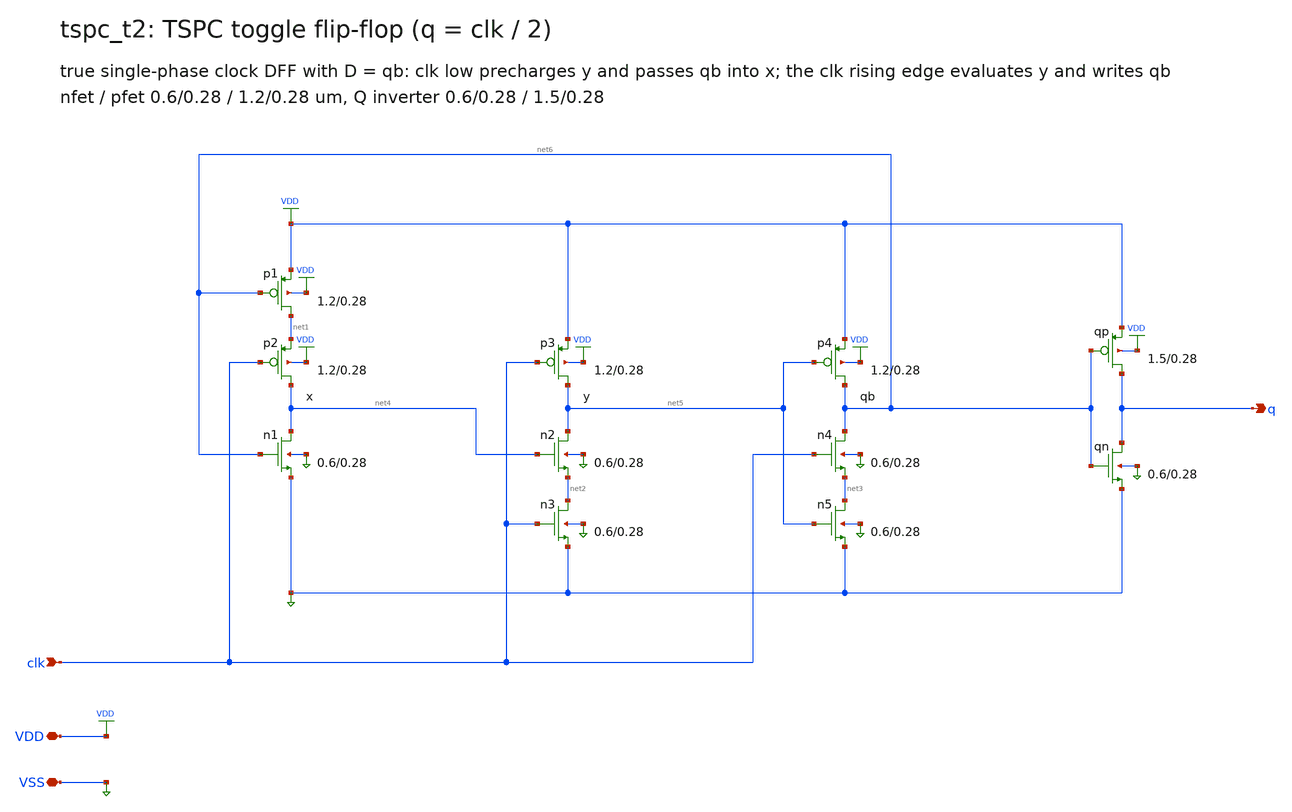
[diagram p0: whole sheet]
** sch_path: xschem/tspc_t2.sch
**.subckt tspc_t2 VDD VSS clk q
*.iopin VDD
*.iopin VSS
*.ipin clk
*.opin q
Xp1 net1 net6 VDD VDD pfet_03v3 L=0.28u W=1.2u nf=1 ad=0.6p as=0.6p pd=3.4u ps=3.4u nrd=0 nrs=0 sa=0
+ sb=0 sd=0 m=1
Xp2 net4 clk net1 VDD pfet_03v3 L=0.28u W=1.2u nf=1 ad=0.6p as=0.6p pd=3.4u ps=3.4u nrd=0 nrs=0 sa=0
+ sb=0 sd=0 m=1
Xn1 net4 net6 VSS VSS nfet_03v3 L=0.28u W=0.6u nf=1 ad=0.3p as=0.3p pd=2.2u ps=2.2u nrd=0 nrs=0 sa=0
+ sb=0 sd=0 m=1
Xp3 net5 clk VDD VDD pfet_03v3 L=0.28u W=1.2u nf=1 ad=0.6p as=0.6p pd=3.4u ps=3.4u nrd=0 nrs=0 sa=0
+ sb=0 sd=0 m=1
Xn2 net5 net4 net2 VSS nfet_03v3 L=0.28u W=0.6u nf=1 ad=0.3p as=0.3p pd=2.2u ps=2.2u nrd=0 nrs=0
+ sa=0 sb=0 sd=0 m=1
Xn3 net2 clk VSS VSS nfet_03v3 L=0.28u W=0.6u nf=1 ad=0.3p as=0.3p pd=2.2u ps=2.2u nrd=0 nrs=0 sa=0
+ sb=0 sd=0 m=1
Xp4 net6 net5 VDD VDD pfet_03v3 L=0.28u W=1.2u nf=1 ad=0.6p as=0.6p pd=3.4u ps=3.4u nrd=0 nrs=0 sa=0
+ sb=0 sd=0 m=1
Xn4 net6 clk net3 VSS nfet_03v3 L=0.28u W=0.6u nf=1 ad=0.3p as=0.3p pd=2.2u ps=2.2u nrd=0 nrs=0 sa=0
+ sb=0 sd=0 m=1
Xn5 net3 net5 VSS VSS nfet_03v3 L=0.28u W=0.6u nf=1 ad=0.3p as=0.3p pd=2.2u ps=2.2u nrd=0 nrs=0 sa=0
+ sb=0 sd=0 m=1
Xqp q net6 VDD VDD pfet_03v3 L=0.28u W=1.5u nf=1 ad=0.75p as=0.75p pd=4.0u ps=4.0u nrd=0 nrs=0 sa=0
+ sb=0 sd=0 m=1
Xqn q net6 VSS VSS nfet_03v3 L=0.28u W=0.6u nf=1 ad=0.3p as=0.3p pd=2.2u ps=2.2u nrd=0 nrs=0 sa=0
+ sb=0 sd=0 m=1
**.ends
.end
